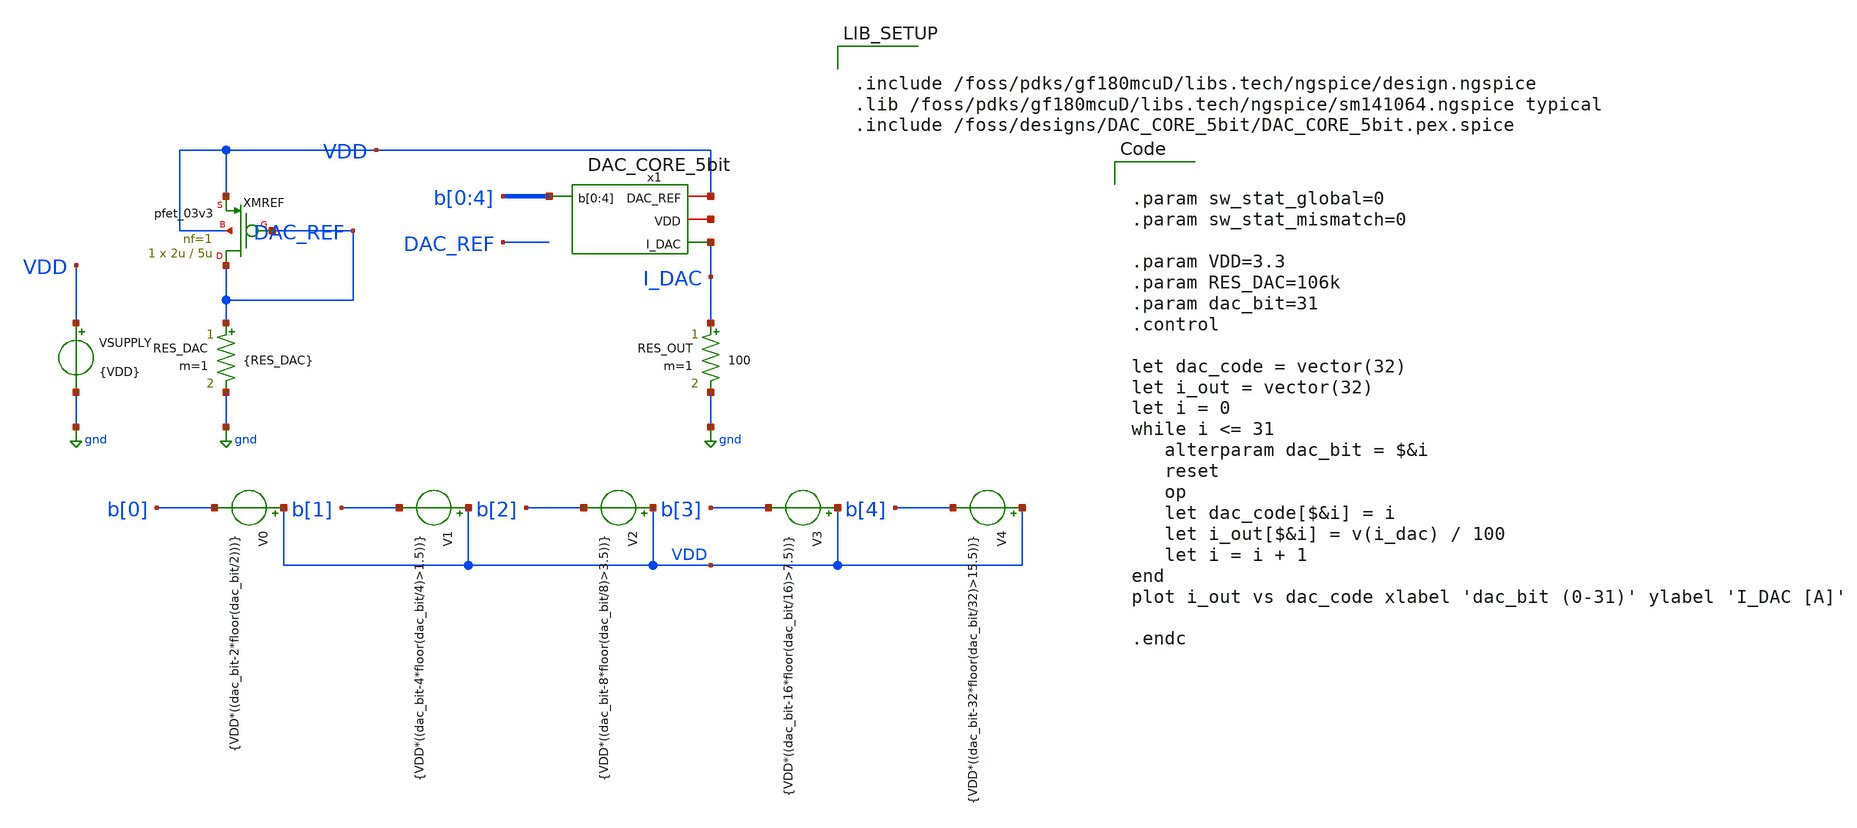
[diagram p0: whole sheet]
** sch_path: DAC_CORE_5bit/DAC_CORE_5bit_test.sch
**.subckt DAC_CORE_5bit_test
XMREF DAC_REF DAC_REF VDD VDD pfet_03v3 L=5u W=2u nf=1 ad='int((nf+1)/2) * W/nf * 0.18u' as='int((nf+2)/2) * W/nf * 0.18u'
+ pd='2*int((nf+1)/2) * (W/nf + 0.18u)' ps='2*int((nf+2)/2) * (W/nf + 0.18u)' nrd='0.18u / W' nrs='0.18u / W'
+ sa=0 sb=0 sd=0 m=1
RES_DAC DAC_REF gnd {RES_DAC} m=1
RES_OUT I_DAC gnd 100 m=1
V0 VDD b[0] {VDD*((dac_bit-2*floor(dac_bit/2)))}
VSUPPLY VDD gnd {VDD}
V1 VDD b[1] {VDD*((dac_bit-4*floor(dac_bit/4)>1.5))}
V2 VDD b[2] {VDD*((dac_bit-8*floor(dac_bit/8)>3.5))}
V3 VDD b[3] {VDD*((dac_bit-16*floor(dac_bit/16)>7.5))}
V4 VDD b[4] {VDD*((dac_bit-32*floor(dac_bit/32)>15.5))}
x1 VDD net1 b[0] b[1] b[2] b[3] b[4] I_DAC DAC_CORE_5bit
**** begin user architecture code


.include /foss/pdks/gf180mcuD/libs.tech/ngspice/design.ngspice
.lib /foss/pdks/gf180mcuD/libs.tech/ngspice/sm141064.ngspice typical
.include /foss/designs/DAC_CORE_5bit/DAC_CORE_5bit.pex.spice




.param sw_stat_global=0
.param sw_stat_mismatch=0

.param VDD=3.3
.param RES_DAC=106k
.param dac_bit=31
.control

let dac_code = vector(32)
let i_out = vector(32)
let i = 0
while i <= 31
   alterparam dac_bit = $&i
   reset
   op
   let dac_code[$&i] = i
   let i_out[$&i] = v(i_dac) / 100
   let i = i + 1
end
plot i_out vs dac_code xlabel 'dac_bit (0-31)' ylabel 'I_DAC [A]'

.endc


**** end user architecture code
**.ends

* expanding   symbol:  DAC_CORE_5bit/DAC_CORE_5bit.sym # of pins=4
** sym_path: DAC_CORE_5bit/DAC_CORE_5bit.sym
** sch_path: DAC_CORE_5bit/DAC_CORE_5bit.sch
.subckt DAC_CORE_5bit DAC_REF VDD b[0] b[1] b[2] b[3] b[4] I_DAC
*.opin I_DAC
*.iopin VDD
*.iopin DAC_REF
*.ipin b[0],b[1],b[2],b[3],b[4]
XMK1 I_DAC b[0] net5 VDD pfet_03v3 L=0.28u W=0.78u nf=1 ad='int((nf+1)/2) * W/nf * 0.18u' as='int((nf+2)/2) * W/nf * 0.18u'
+ pd='2*int((nf+1)/2) * (W/nf + 0.18u)' ps='2*int((nf+2)/2) * (W/nf + 0.18u)' nrd='0.18u / W' nrs='0.18u / W'
+ sa=0 sb=0 sd=0 m=1
XMK2 I_DAC b[1] net1 VDD pfet_03v3 L=0.28u W=0.78u nf=1 ad='int((nf+1)/2) * W/nf * 0.18u' as='int((nf+2)/2) * W/nf * 0.18u'
+ pd='2*int((nf+1)/2) * (W/nf + 0.18u)' ps='2*int((nf+2)/2) * (W/nf + 0.18u)' nrd='0.18u / W' nrs='0.18u / W'
+ sa=0 sb=0 sd=0 m=2
XMK3 I_DAC b[2] net2 VDD pfet_03v3 L=0.28u W=0.78u nf=1 ad='int((nf+1)/2) * W/nf * 0.18u' as='int((nf+2)/2) * W/nf * 0.18u'
+ pd='2*int((nf+1)/2) * (W/nf + 0.18u)' ps='2*int((nf+2)/2) * (W/nf + 0.18u)' nrd='0.18u / W' nrs='0.18u / W'
+ sa=0 sb=0 sd=0 m=4
XMK4 I_DAC b[3] net3 VDD pfet_03v3 L=0.28u W=0.78u nf=1 ad='int((nf+1)/2) * W/nf * 0.18u' as='int((nf+2)/2) * W/nf * 0.18u'
+ pd='2*int((nf+1)/2) * (W/nf + 0.18u)' ps='2*int((nf+2)/2) * (W/nf + 0.18u)' nrd='0.18u / W' nrs='0.18u / W'
+ sa=0 sb=0 sd=0 m=8
XMK5 I_DAC b[4] net4 VDD pfet_03v3 L=0.28u W=0.78u nf=1 ad='int((nf+1)/2) * W/nf * 0.18u' as='int((nf+2)/2) * W/nf * 0.18u'
+ pd='2*int((nf+1)/2) * (W/nf + 0.18u)' ps='2*int((nf+2)/2) * (W/nf + 0.18u)' nrd='0.18u / W' nrs='0.18u / W'
+ sa=0 sb=0 sd=0 m=16
XM1 net5 DAC_REF VDD VDD pfet_03v3 L=2u W=5u nf=1 ad='int((nf+1)/2) * W/nf * 0.18u' as='int((nf+2)/2) * W/nf * 0.18u'
+ pd='2*int((nf+1)/2) * (W/nf + 0.18u)' ps='2*int((nf+2)/2) * (W/nf + 0.18u)' nrd='0.18u / W' nrs='0.18u / W'
+ sa=0 sb=0 sd=0 m=1
XM2 net1 DAC_REF VDD VDD pfet_03v3 L=2u W=5u nf=1 ad='int((nf+1)/2) * W/nf * 0.18u' as='int((nf+2)/2) * W/nf * 0.18u'
+ pd='2*int((nf+1)/2) * (W/nf + 0.18u)' ps='2*int((nf+2)/2) * (W/nf + 0.18u)' nrd='0.18u / W' nrs='0.18u / W'
+ sa=0 sb=0 sd=0 m=2
XM3 net2 DAC_REF VDD VDD pfet_03v3 L=2u W=5u nf=1 ad='int((nf+1)/2) * W/nf * 0.18u' as='int((nf+2)/2) * W/nf * 0.18u'
+ pd='2*int((nf+1)/2) * (W/nf + 0.18u)' ps='2*int((nf+2)/2) * (W/nf + 0.18u)' nrd='0.18u / W' nrs='0.18u / W'
+ sa=0 sb=0 sd=0 m=4
XM4 net3 DAC_REF VDD VDD pfet_03v3 L=2u W=5u nf=1 ad='int((nf+1)/2) * W/nf * 0.18u' as='int((nf+2)/2) * W/nf * 0.18u'
+ pd='2*int((nf+1)/2) * (W/nf + 0.18u)' ps='2*int((nf+2)/2) * (W/nf + 0.18u)' nrd='0.18u / W' nrs='0.18u / W'
+ sa=0 sb=0 sd=0 m=8
XM5 net4 DAC_REF VDD VDD pfet_03v3 L=2u W=5u nf=1 ad='int((nf+1)/2) * W/nf * 0.18u' as='int((nf+2)/2) * W/nf * 0.18u'
+ pd='2*int((nf+1)/2) * (W/nf + 0.18u)' ps='2*int((nf+2)/2) * (W/nf + 0.18u)' nrd='0.18u / W' nrs='0.18u / W'
+ sa=0 sb=0 sd=0 m=16
.ends

.GLOBAL gnd
.end
